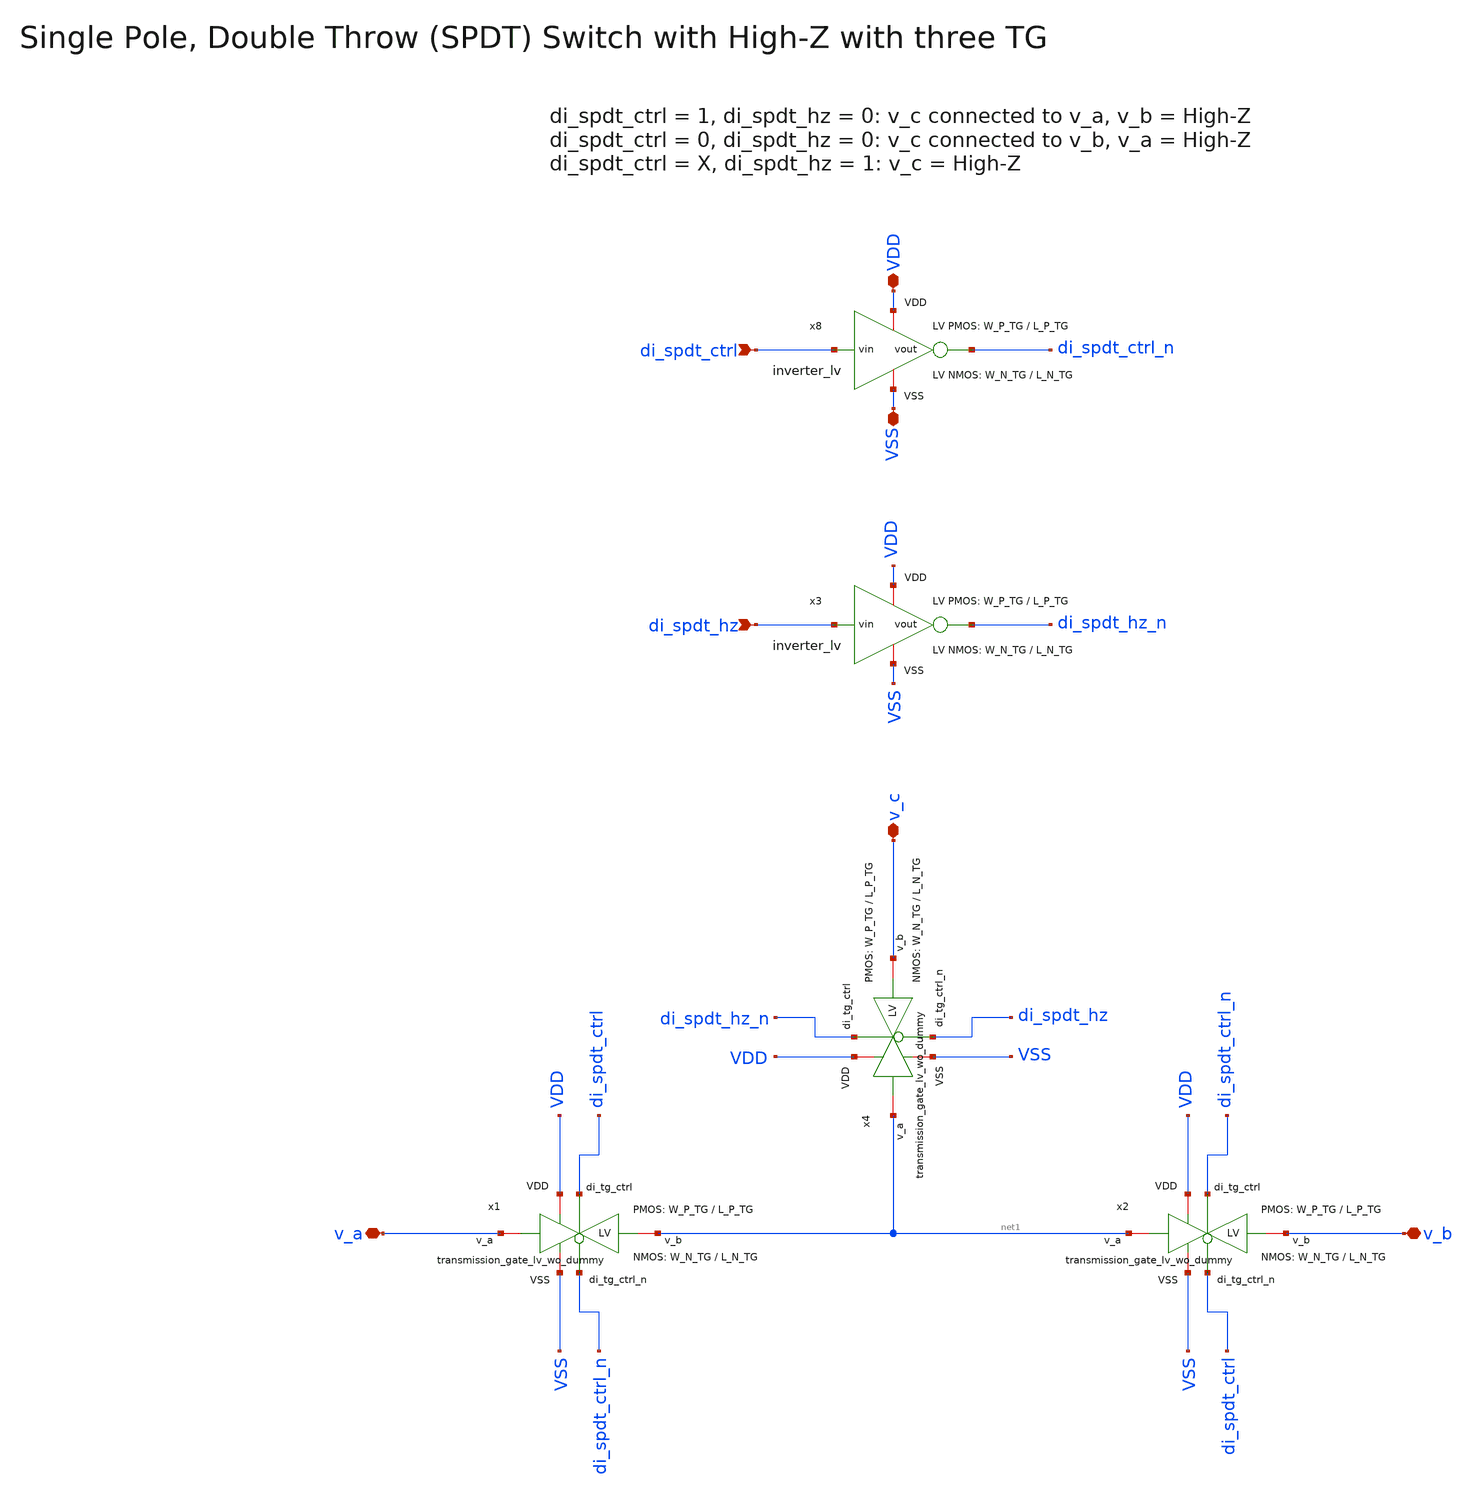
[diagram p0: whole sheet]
** sch_path: SG13G2_ATBS-ADC-main/xschem/spdt_switch/spdt_hz_switch.sch
**.subckt spdt_hz_switch v_a v_b v_c VDD VSS di_spdt_ctrl di_spdt_hz
*.iopin v_a
*.iopin v_b
*.iopin v_c
*.iopin VDD
*.iopin VSS
*.ipin di_spdt_ctrl
*.ipin di_spdt_hz
x1 VDD di_spdt_ctrl VSS net1 v_a di_spdt_ctrl_n transmission_gate_lv_wo_dummy W_P=W_P_TG L_P=L_P_TG
+ W_N=W_N_TG L_N=L_N_TG
x2 VDD di_spdt_ctrl_n VSS v_b net1 di_spdt_ctrl transmission_gate_lv_wo_dummy W_P=W_P_TG L_P=L_P_TG
+ W_N=W_N_TG L_N=L_N_TG
x8 VDD di_spdt_ctrl di_spdt_ctrl_n VSS inverter_lv W_P=W_P_TG L_P=L_P_TG W_N=W_N_TG L_N=L_N_TG
x3 VDD di_spdt_hz di_spdt_hz_n VSS inverter_lv W_P=W_P_TG L_P=L_P_TG W_N=W_N_TG L_N=L_N_TG
x4 VDD di_spdt_hz_n VSS v_c net1 di_spdt_hz transmission_gate_lv_wo_dummy W_P=W_P_TG L_P=L_P_TG
+ W_N=W_N_TG L_N=L_N_TG
**.ends

* expanding   symbol:  transmission_gate/transmission_gate_lv_wo_dummy.sym # of pins=6
** sym_path: SG13G2_ATBS-ADC-main/xschem/transmission_gate/transmission_gate_lv_wo_dummy.sym
** sch_path: SG13G2_ATBS-ADC-main/xschem/transmission_gate/transmission_gate_lv_wo_dummy.sch
.subckt transmission_gate_lv_wo_dummy VDD di_tg_ctrl VSS v_b v_a di_tg_ctrl_n  W_P=1.0u L_P=0.13u
+ W_N=1.0u L_N=0.13u
*.iopin v_a
*.iopin v_b
*.iopin VDD
*.iopin VSS
*.ipin di_tg_ctrl
*.ipin di_tg_ctrl_n
XM1 v_a di_tg_ctrl v_b VSS sg13_lv_nmos w=W_N l=L_N ng=1 m=1 mm_ok=1
XM2 v_a di_tg_ctrl_n v_b VDD sg13_lv_pmos w=W_P l=L_P ng=1 m=1 mm_ok=1
.ends


* expanding   symbol:  inverter/inverter_lv.sym # of pins=4
** sym_path: SG13G2_ATBS-ADC-main/xschem/inverter/inverter_lv.sym
** sch_path: SG13G2_ATBS-ADC-main/xschem/inverter/inverter_lv.sch
.subckt inverter_lv VDD vin vout VSS  W_P=3.0u L_P=0.13u W_N=1.0u L_N=0.13u
*.ipin vin
*.iopin VDD
*.iopin VSS
*.opin vout
XM1 vout vin VDD VDD sg13_lv_pmos w=W_P l=L_P ng=1 m=1 mm_ok=1
XM2 vout vin VSS VSS sg13_lv_nmos w=W_N l=L_N ng=1 m=1 mm_ok=1
.ends

.end
